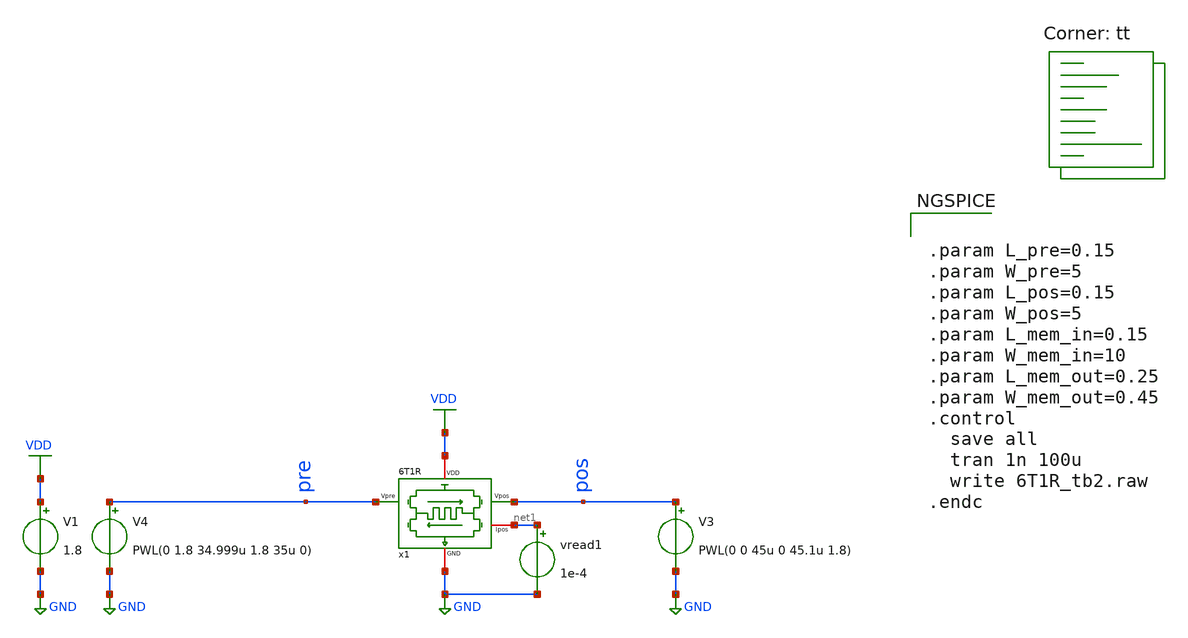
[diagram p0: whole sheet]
** sch_path: synapse/6T1R_tb.sch
**.subckt 6T1R_tb
V1 VDD GND 1.8
V3 pos GND PWL(0 0 45u 0 45.1u 1.8)
vread1 net1 GND 1e-4
x1 VDD net1 pre pos GND 6T1R
V4 pre GND PWL(0 1.8 34.999u 1.8 35u 0)
**** begin user architecture code
.lib $::SKYWATER_MODELS/sky130.lib.spice tt

** opencircuitdesign pdks install
.inc $::SKYWATER_MODELS/rram_v0.spice



.param L_pre=0.15
.param W_pre=5
.param L_pos=0.15
.param W_pos=5
.param L_mem_in=0.15
.param W_mem_in=10
.param L_mem_out=0.25
.param W_mem_out=0.45
.control
  save all
  tran 1n 100u
  write 6T1R_tb2.raw
.endc


**** end user architecture code
**.ends

* expanding   symbol:  /home/ricardo/RATT_repos/Proyectos_xschem/synapse/6T1R.sym # of pins=5
** sym_path: synapse/6T1R.sym
** sch_path: synapse/6T1R.sch
.subckt 6T1R VDD Ipos Vpre Vpos GND
*.ipin Vpre
*.ipin Vpos
*.iopin GND
*.iopin Ipos
*.iopin VDD
XM1 vipre Vpre net1 GND sky130_fd_pr__nfet_01v8 L={L_pre} W={W_pre} nf=1 ad='int((nf+1)/2) * W/nf * 0.29'
+ as='int((nf+2)/2) * W/nf * 0.29' pd='2*int((nf+1)/2) * (W/nf + 0.29)' ps='2*int((nf+2)/2) * (W/nf + 0.29)'
+ nrd='0.29 / W' nrs='0.29 / W' sa=0 sb=0 sd=0 mult=1 m=1
XM3 vipre Vpos net2 GND sky130_fd_pr__nfet_01v8 L={L_pos} W={W_pos} nf=1 ad='int((nf+1)/2) * W/nf * 0.29'
+ as='int((nf+2)/2) * W/nf * 0.29' pd='2*int((nf+1)/2) * (W/nf + 0.29)' ps='2*int((nf+2)/2) * (W/nf + 0.29)'
+ nrd='0.29 / W' nrs='0.29 / W' sa=0 sb=0 sd=0 mult=1 m=1
XM6 Ipos vipre VDD VDD sky130_fd_pr__pfet_01v8 L={L_mem_out} W={W_mem_out} nf=1 ad='int((nf+1)/2) * W/nf * 0.29'
+ as='int((nf+2)/2) * W/nf * 0.29' pd='2*int((nf+1)/2) * (W/nf + 0.29)' ps='2*int((nf+2)/2) * (W/nf + 0.29)'
+ nrd='0.29 / W' nrs='0.29 / W' sa=0 sb=0 sd=0 mult=1 m=1
XM5 vipre vipre VDD VDD sky130_fd_pr__pfet_01v8 L={L_mem_in} W={W_mem_in} nf=1 ad='int((nf+1)/2) * W/nf * 0.29'
+ as='int((nf+2)/2) * W/nf * 0.29' pd='2*int((nf+1)/2) * (W/nf + 0.29)' ps='2*int((nf+2)/2) * (W/nf + 0.29)'
+ nrd='0.29 / W' nrs='0.29 / W' sa=0 sb=0 sd=0 mult=1 m=1
XM2 net1 Vpos GND GND sky130_fd_pr__nfet_01v8 L={L_pos} W={W_pos} nf=1 ad='int((nf+1)/2) * W/nf * 0.29'
+ as='int((nf+2)/2) * W/nf * 0.29' pd='2*int((nf+1)/2) * (W/nf + 0.29)' ps='2*int((nf+2)/2) * (W/nf + 0.29)'
+ nrd='0.29 / W' nrs='0.29 / W' sa=0 sb=0 sd=0 mult=1 m=1
XM4 net2 Vpre GND GND sky130_fd_pr__nfet_01v8 L={L_pre} W={W_pre} nf=1 ad='int((nf+1)/2) * W/nf * 0.29'
+ as='int((nf+2)/2) * W/nf * 0.29' pd='2*int((nf+1)/2) * (W/nf + 0.29)' ps='2*int((nf+2)/2) * (W/nf + 0.29)'
+ nrd='0.29 / W' nrs='0.29 / W' sa=0 sb=0 sd=0 mult=1 m=1
XR1 net2 net1 rram_v0
.ends

.GLOBAL GND
.GLOBAL VDD
.end
